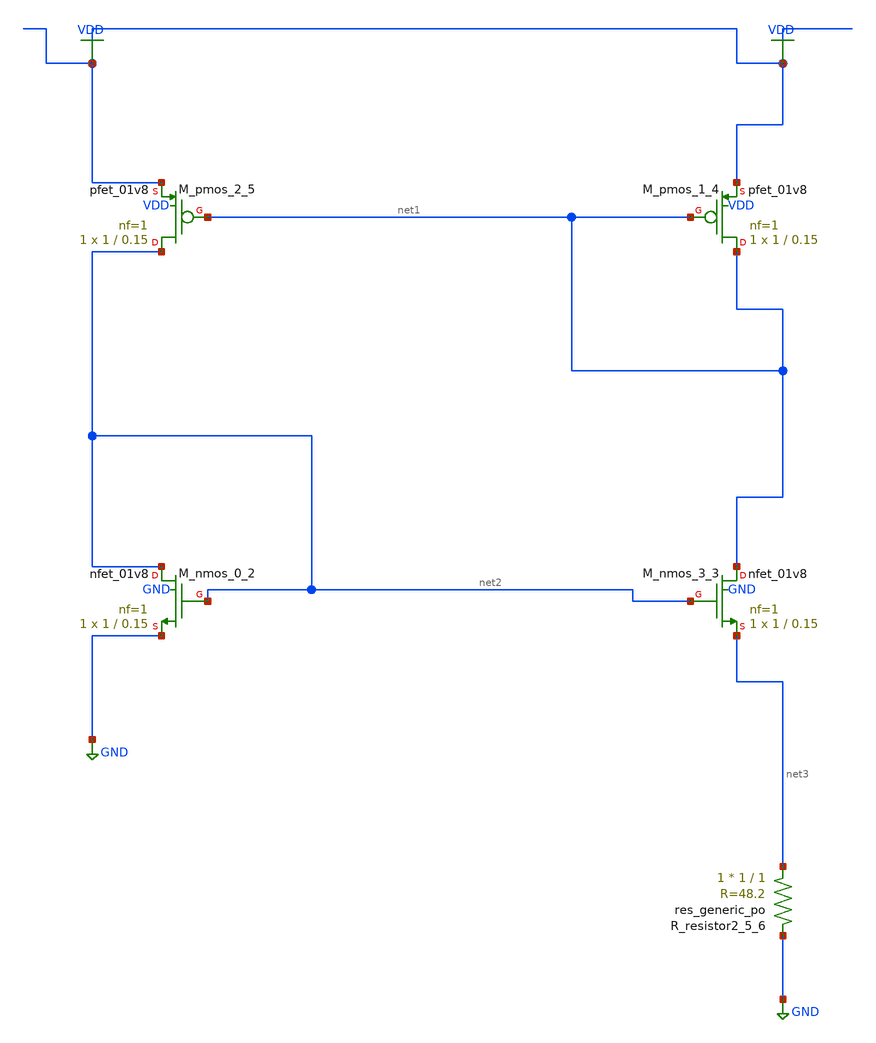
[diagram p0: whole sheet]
** sch_path: schematics/AMSNet/762.sch
**.subckt 762
XM_nmos_0_2 net2 net2 GND GND sky130_fd_pr__nfet_01v8 L=0.15 W=1 nf=1 ad='int((1 + 1)/2) * 1 / 1 * 0.29'
+ as='int((1 + 2)/2) * 1 / 1 * 0.29' pd='2*int((1 + 1)/2) * (1 / 1 + 0.29)' ps='2*int((1 + 2)/2) * (1 / 1 + 0.29)'
+ nrd='0.29 / 1 ' nrs='0.29 / 1 ' sa=0 sb=0 sd=0 mult=1 m=1
XM_nmos_3_3 net1 net2 net3 GND sky130_fd_pr__nfet_01v8 L=0.15 W=1 nf=1 ad='int((1 + 1)/2) * 1 / 1 * 0.29'
+ as='int((1 + 2)/2) * 1 / 1 * 0.29' pd='2*int((1 + 1)/2) * (1 / 1 + 0.29)' ps='2*int((1 + 2)/2) * (1 / 1 + 0.29)'
+ nrd='0.29 / 1 ' nrs='0.29 / 1 ' sa=0 sb=0 sd=0 mult=1 m=1
XM_pmos_1_4 net1 net1 VDD VDD sky130_fd_pr__pfet_01v8 L=0.15 W=1 nf=1 ad='int((1 + 1)/2) * 1 / 1 * 0.29'
+ as='int((1 + 2)/2) * 1 / 1 * 0.29' pd='2*int((1 + 1)/2) * (1 / 1 + 0.29)' ps='2*int((1 + 2)/2) * (1 / 1 + 0.29)'
+ nrd='0.29 / 1 ' nrs='0.29 / 1 ' sa=0 sb=0 sd=0 mult=1 m=1
XM_pmos_2_5 net2 net1 VDD VDD sky130_fd_pr__pfet_01v8 L=0.15 W=1 nf=1 ad='int((1 + 1)/2) * 1 / 1 * 0.29'
+ as='int((1 + 2)/2) * 1 / 1 * 0.29' pd='2*int((1 + 1)/2) * (1 / 1 + 0.29)' ps='2*int((1 + 2)/2) * (1 / 1 + 0.29)'
+ nrd='0.29 / 1 ' nrs='0.29 / 1 ' sa=0 sb=0 sd=0 mult=1 m=1
XR_resistor2_5_6 net3 GND sky130_fd_pr__res_generic_po W=1 L=1 m=1
**.ends
.GLOBAL GND
.GLOBAL VDD
.end
